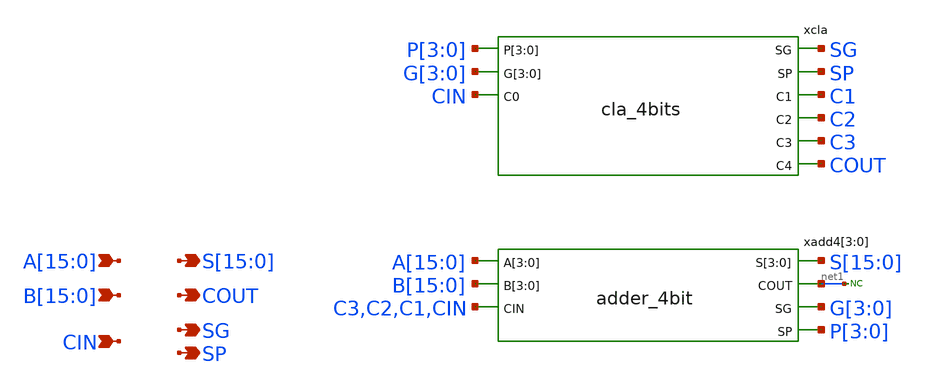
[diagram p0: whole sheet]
** sch_path: sky130A/xschem_libs/sky130_tests/adder_16bit/schematic/adder_16bit.sch
**.subckt adder_16bit
*+ A[15],A[14],A[13],A[12],A[11],A[10],A[9],A[8],A[7],A[6],A[5],A[4],A[3],A[2],A[1],A[0] B[15],B[14],B[13],B[12],B[11],B[10],B[9],B[8],B[7],B[6],B[5],B[4],B[3],B[2],B[1],B[0] CIN
*+ S[15],S[14],S[13],S[12],S[11],S[10],S[9],S[8],S[7],S[6],S[5],S[4],S[3],S[2],S[1],S[0] SP SG COUT
*.ipin A[15],A[14],A[13],A[12],A[11],A[10],A[9],A[8],A[7],A[6],A[5],A[4],A[3],A[2],A[1],A[0]
*.ipin B[15],B[14],B[13],B[12],B[11],B[10],B[9],B[8],B[7],B[6],B[5],B[4],B[3],B[2],B[1],B[0]
*.ipin CIN
*.opin S[15],S[14],S[13],S[12],S[11],S[10],S[9],S[8],S[7],S[6],S[5],S[4],S[3],S[2],S[1],S[0]
*.opin SP
*.opin SG
*.opin COUT
xadd4[3] A[15] A[14] A[13] A[12] S[15] S[14] S[13] S[12] B[15] B[14] B[13] B[12] net1 G[3] C3 P[3]
+ adder_4bit
xadd4[2] A[11] A[10] A[9] A[8] S[11] S[10] S[9] S[8] B[11] B[10] B[9] B[8] net1 G[2] C2 P[2]
+ adder_4bit
xadd4[1] A[7] A[6] A[5] A[4] S[7] S[6] S[5] S[4] B[7] B[6] B[5] B[4] net1 G[1] C1 P[1] adder_4bit
xadd4[0] A[3] A[2] A[1] A[0] S[3] S[2] S[1] S[0] B[3] B[2] B[1] B[0] net1 G[0] CIN P[0] adder_4bit
xcla SG SP C1 P[3] P[2] P[1] P[0] C2 G[3] G[2] G[1] G[0] C3 COUT CIN cla_4bits
* noconn #net1
**.ends

* expanding   symbol:  sky130_tests/adder_4bit.sym # of pins=7
** sym_path: sky130_tests/adder_4bit.sym
** sch_path: sky130_tests/adder_4bit.sch
.subckt adder_4bit A[3] A[2] A[1] A[0] S[3] S[2] S[1] S[0] B[3] B[2] B[1] B[0] COUT SG CIN SP
*.ipin A[3],A[2],A[1],A[0]
*.ipin B[3],B[2],B[1],B[0]
*.ipin CIN
*.opin S[3],S[2],S[1],S[0]
*.opin SP
*.opin SG
*.opin COUT
xcla SG SP C1 P[3] P[2] P[1] P[0] C2 G[3] G[2] G[1] G[0] C3 COUT CIN cla_4bits
xadd1[3] S[3] A[3] B[3] G[3] C3 P[3] adder_1bit
xadd1[2] S[2] A[2] B[2] G[2] C2 P[2] adder_1bit
xadd1[1] S[1] A[1] B[1] G[1] C1 P[1] adder_1bit
xadd1[0] S[0] A[0] B[0] G[0] CIN P[0] adder_1bit
.ends


* expanding   symbol:  sky130_tests/cla_4bits.sym # of pins=9
** sym_path: sky130_tests/cla_4bits.sym
** sch_path: sky130_tests/cla_4bits.sch
.subckt cla_4bits SG SP C1 P[3] P[2] P[1] P[0] C2 G[3] G[2] G[1] G[0] C3 C4 C0
*.ipin P[3],P[2],P[1],P[0]
*.ipin G[3],G[2],G[1],G[0]
*.ipin C0
*.opin C4
*.opin C3
*.opin C2
*.opin C1
*.opin SG
*.opin SP
x1 P[0] VSS VSS VCC VCC net4 sky130_fd_sc_hd__inv_1
x2 net5 VSS VSS VCC VCC C1 sky130_fd_sc_hd__inv_1
x3 P[1] VSS VSS VCC VCC net2 sky130_fd_sc_hd__inv_1
x4 net8 VSS VSS VCC VCC C3 sky130_fd_sc_hd__inv_1
x5 G[1] VSS VSS VCC VCC net3 sky130_fd_sc_hd__inv_1
x6 net12 VSS VSS VCC VCC net13 sky130_fd_sc_hd__inv_1
x7 G[1] P[2] G[2] VSS VSS VCC VCC net12 sky130_fd_sc_hd__a21oi_1
x8 P[3] net13 G[3] VSS VSS VCC VCC net14 sky130_fd_sc_hd__a21oi_1
x9 C0 P[0] G[0] VSS VSS VCC VCC net5 sky130_fd_sc_hd__a21oi_1
x10 P[2] C2 G[2] VSS VSS VCC VCC net8 sky130_fd_sc_hd__a21oi_1
x11 G[0] VSS VSS VCC VCC net1 sky130_fd_sc_hd__inv_1
x12 net2 net5 net3 VSS VSS VCC VCC C2 sky130_fd_sc_hd__o21ai_1
x13 net5 net10 net14 VSS VSS VCC VCC C4 sky130_fd_sc_hd__o21ai_1
x14 net1 net10 net14 VSS VSS VCC VCC SG sky130_fd_sc_hd__o21ai_1
x15 net4 net10 VSS VSS VCC VCC SP sky130_fd_sc_hd__nor2_1
x16 P[1] P[2] P[3] VSS VSS VCC VCC net10 sky130_fd_sc_hd__nand3_1
C2 net4 0 5f m=1
C1 net10 0 5f m=1
C3 net1 0 5f m=1
C4 net14 0 5f m=1
C5 net2 0 5f m=1
C6 net5 0 5f m=1
C7 net3 0 5f m=1
C8 net8 0 5f m=1
C9 net13 0 5f m=1
C10 net12 0 5f m=1
C19[3] P[3] 0 5f m=1
C19[2] P[2] 0 5f m=1
C19[1] P[1] 0 5f m=1
C19[0] P[0] 0 5f m=1
C18[3] G[3] 0 5f m=1
C18[2] G[2] 0 5f m=1
C18[1] G[1] 0 5f m=1
C18[0] G[0] 0 5f m=1
C17 C0 0 5f m=1
.ends


* expanding   symbol:  sky130_tests/adder_1bit.sym # of pins=6
** sym_path: sky130_tests/adder_1bit.sym
** sch_path: sky130_tests/adder_1bit.sch
.subckt adder_1bit S A B G CIN P
*.ipin A
*.ipin B
*.ipin CIN
*.opin S
*.opin P
*.opin G
x4 A B VSS VSS VCC VCC G sky130_fd_sc_hd__and2_1
x2 A B VSS VSS VCC VCC P sky130_fd_sc_hd__xor2_1
x3 P CIN VSS VSS VCC VCC S sky130_fd_sc_hd__xor2_1
C1 G 0 5f m=1
C2 P 0 5f m=1
C3 S 0 5f m=1
.ends

.end
